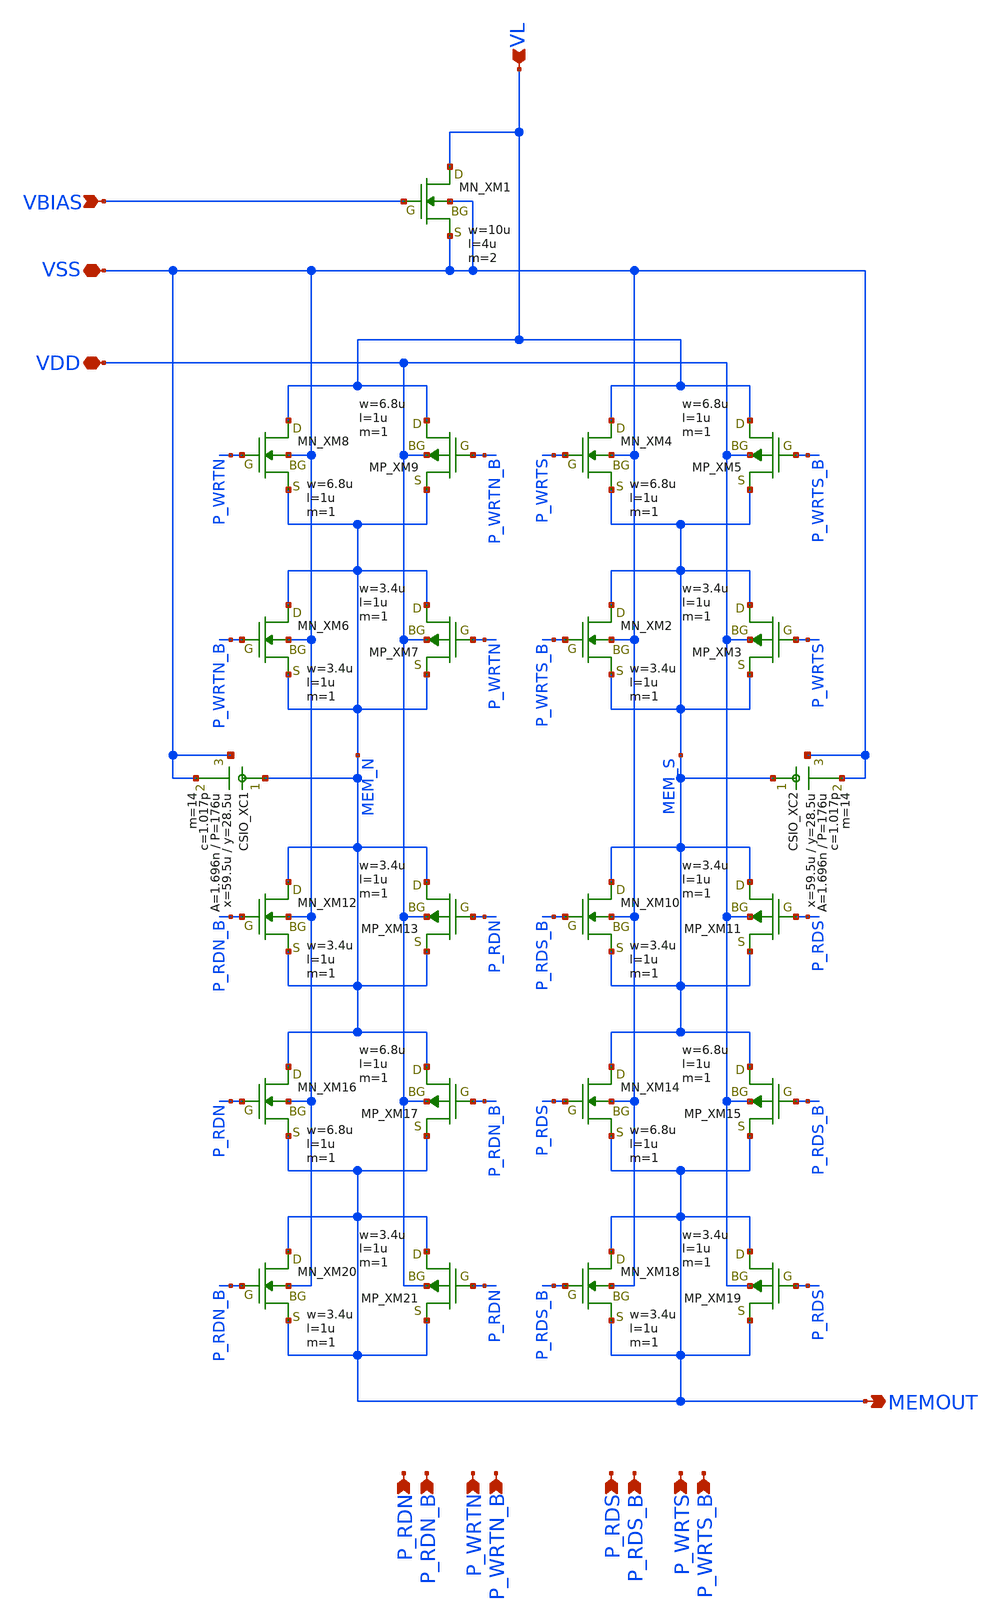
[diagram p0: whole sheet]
** sch_path: member_project/imager/YuMaehashi/design/readout_unit.sch
**.subckt readout_unit VL VSS VBIAS MEMOUT P_RDN P_RDN_B P_WRTN P_WRTN_B P_RDS P_RDS_B P_WRTS
*+ P_WRTS_B VDD
*.ipin VL
*.iopin VSS
*.ipin VBIAS
*.opin MEMOUT
*.ipin P_RDN
*.ipin P_RDN_B
*.ipin P_WRTN
*.ipin P_WRTN_B
*.ipin P_RDS
*.ipin P_RDS_B
*.ipin P_WRTS
*.ipin P_WRTS_B
*.iopin VDD
XXM1 VL VBIAS VSS VSS NMOS w=10u l=4u nrd=0 nrs=0 m=2
XXC1 MEM_N VSS VSS F_CSIO c=1.017p x=59.5u y=28.5u m=14
XXC2 MEM_S VSS VSS F_CSIO c=1.017p x=59.5u y=28.5u m=14
XXM2 MEM_S P_WRTS_B MEM_S VSS NMOS w=3.4u l=1u nrd=0 nrs=0 m=1
XXM3 MEM_S P_WRTS MEM_S VDD PMOS w=3.4u l=1u nrd=0 nrs=0 m=1
XXM4 VL P_WRTS MEM_S VSS NMOS w=6.8u l=1u nrd=0 nrs=0 m=1
XXM5 VL P_WRTS_B MEM_S VDD PMOS w=6.8u l=1u nrd=0 nrs=0 m=1
XXM6 MEM_N P_WRTN_B MEM_N VSS NMOS w=3.4u l=1u nrd=0 nrs=0 m=1
XXM7 MEM_N P_WRTN MEM_N VDD PMOS w=3.4u l=1u nrd=0 nrs=0 m=1
XXM8 VL P_WRTN MEM_N VSS NMOS w=6.8u l=1u nrd=0 nrs=0 m=1
XXM9 VL P_WRTN_B MEM_N VDD PMOS w=6.8u l=1u nrd=0 nrs=0 m=1
XXM10 MEM_S P_RDS_B MEM_S VSS NMOS w=3.4u l=1u nrd=0 nrs=0 m=1
XXM11 MEM_S P_RDS MEM_S VDD PMOS w=3.4u l=1u nrd=0 nrs=0 m=1
XXM12 MEM_N P_RDN_B MEM_N VSS NMOS w=3.4u l=1u nrd=0 nrs=0 m=1
XXM13 MEM_N P_RDN MEM_N VDD PMOS w=3.4u l=1u nrd=0 nrs=0 m=1
XXM14 MEM_S P_RDS MEMOUT VSS NMOS w=6.8u l=1u nrd=0 nrs=0 m=1
XXM15 MEM_S P_RDS_B MEMOUT VDD PMOS w=6.8u l=1u nrd=0 nrs=0 m=1
XXM16 MEM_N P_RDN MEMOUT VSS NMOS w=6.8u l=1u nrd=0 nrs=0 m=1
XXM17 MEM_N P_RDN_B MEMOUT VDD PMOS w=6.8u l=1u nrd=0 nrs=0 m=1
XXM18 MEMOUT P_RDS_B MEMOUT VSS NMOS w=3.4u l=1u nrd=0 nrs=0 m=1
XXM19 MEMOUT P_RDS MEMOUT VDD PMOS w=3.4u l=1u nrd=0 nrs=0 m=1
XXM20 MEMOUT P_RDN_B MEMOUT VSS NMOS w=3.4u l=1u nrd=0 nrs=0 m=1
XXM21 MEMOUT P_RDN MEMOUT VDD PMOS w=3.4u l=1u nrd=0 nrs=0 m=1
**.ends
.end
